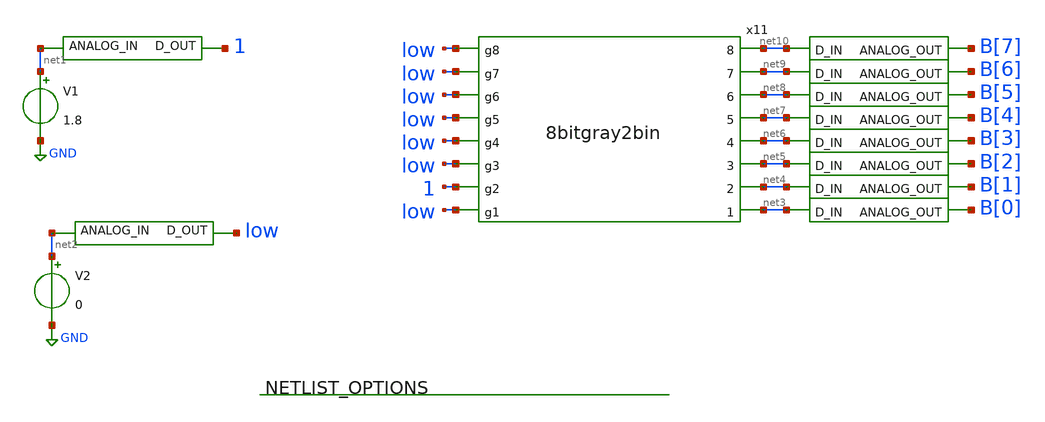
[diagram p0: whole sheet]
** sch_path: xschem/testbench/gray_count_tb.sch
**.subckt gray_count_tb
x11 net10 low low net9 net8 low net7 low low net6 net5 low 1 net4 low net3 8bitgray2bin
V1 net1 GND 1.8
x1 1 net1 adc_bridge
V2 net2 GND 0
x2 low net2 adc_bridge
x12 B[7] net10 dac_bridge
x13 B[6] net9 dac_bridge
x14 B[5] net8 dac_bridge
x16 B[4] net7 dac_bridge
x17 B[3] net6 dac_bridge
x18 B[2] net5 dac_bridge
x19 B[1] net4 dac_bridge
x37 B[0] net3 dac_bridge
**.ends

* expanding   symbol:  adc/8bitgray2bin.sym # of pins=16
** sym_path: xschem/adc/8bitgray2bin.sym
** sch_path: xschem/adc/8bitgray2bin.sch
.subckt 8bitgray2bin 8 g8 g7 7 6 g6 5 g5 g4 4 3 g3 g2 2 g1 1
*.opin 7
*.opin 6
*.opin 5
*.opin 4
*.opin 3
*.opin 2
*.opin 1
*.opin 8
*.ipin g5
*.ipin g4
*.ipin g3
*.ipin g8
*.ipin g7
*.ipin g6
*.ipin g2
*.ipin g1
**** begin user architecture code


* lsb first.
a1 [g1 g2 g3 g4 g5 g6 g7 g8] [1 2 3 4 5 6 7 8] gray2bin_lut
.model gray2bin_lut d_genlut(rise_delay=[1p 1p] fall_delay=[1p 1p]  input_load=[1p 1p]
+ input_delay=[0 0]
+ table_values=01101001100101101001011001101001100101100110100101101001100101101001011001101001011010011001011001101001100101101001011001101001100101100110100101101001100101100110100110010110100101100110100101101001100101101001011001101001100101100110100101101001100101100011110011000011110000110011110011000011001111000011110011000011110000110011110000111100110000110011110011000011110000110011110011000011001111000011110011000011001111001100001111000011001111000011110011000011110000110011110011000011001111000011110011000011000011111111000011110000000011111111000000001111000011111111000011110000000011110000111111110000000011111111000011110000000011111111000000001111000011111111000000001111111100001111000000001111000011111111000011110000000011111111000000001111000011111111000000000000111111111111111100000000111111110000000000000000111111111111111100000000000000001111111100000000111111111111111100000000111111110000000000000000111111110000000011111111111111110000000000000000111111111111111100000000111111110000000000000000111111110000000000000000111111111111111111111111111111110000000000000000111111111111111100000000000000000000000000000000111111111111111111111111111111110000000000000000000000000000000011111111111111110000000000000000111111111111111111111111111111110000000000000000000000000000000000000000000000001111111111111111111111111111111111111111111111111111111111111111000000000000000000000000000000001111111111111111111111111111111100000000000000000000000000000000000000000000000000000000000000001111111111111111111111111111111100000000000000000000000000000000000000000000000000000000000000001111111111111111111111111111111111111111111111111111111111111111111111111111111111111111111111111111111111111111111111111111111100000000000000000000000000000000000000000000000000000000000000000000000000000000000000000000000000000000000000000000000000000000000000000000000000000000000000000000000000000000000000000000000011111111111111111111111111111111111111111111111111111111111111111111111111111111111111111111111111111111111111111111111111111111)




**** end user architecture code
.ends


* expanding   symbol:  digital_prims/adc_bridge.sym # of pins=2
** sym_path: xschem/digital_prims/adc_bridge.sym
** sch_path: xschem/digital_prims/adc_bridge.sch
.subckt adc_bridge D_OUT ANALOG_IN
*.ipin ANALOG_IN
*.opin D_OUT
**** begin user architecture code


abridge [ANALOG_IN] [D_OUT] adc_buff
.model adc_buff adc_bridge(in_low=0.9 in_high =0.9)


**** end user architecture code
.ends


* expanding   symbol:  digital_prims/dac_bridge.sym # of pins=2
** sym_path: xschem/digital_prims/dac_bridge.sym
** sch_path: xschem/digital_prims/dac_bridge.sch
.subckt dac_bridge ANALOG_OUT D_IN
*.ipin D_IN
*.opin ANALOG_OUT
**** begin user architecture code


abridge_d [D_IN] [ANALOG_OUT] dac_buff
.model dac_buff dac_bridge(out_high=1.8)


**** end user architecture code
.ends

.GLOBAL GND
**** begin user architecture code


.control
save all

*dc v2 0 1.8 0.05
*plot v(test)
tran 1u 5u
write gray_count_tb.raw
.endc


**** end user architecture code
.end
